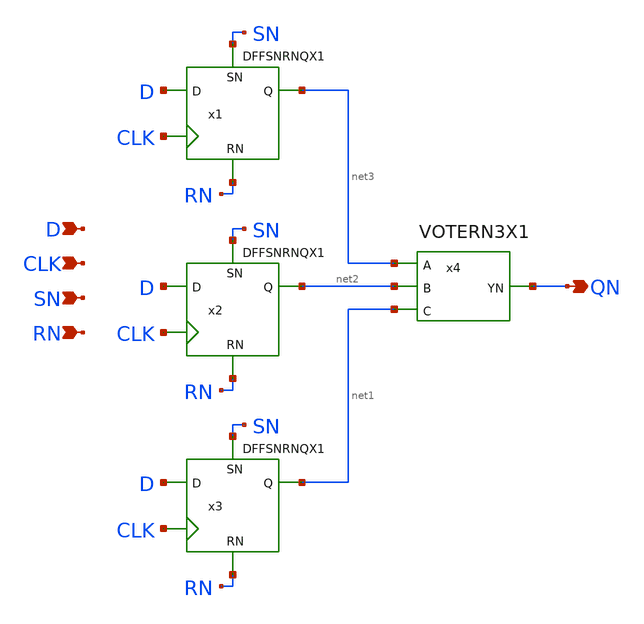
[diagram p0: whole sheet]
** sch_path: lib/xschem/TMRDFFSNRNQNX1.sch
**.subckt TMRDFFSNRNQNX1 QN D CLK SN RN
*.opin QN
*.ipin D
*.ipin CLK
*.ipin SN
*.ipin RN
x4 net3 net2 net1 QN VDD VSS VOTERN3X1
x1 net3 D CLK SN RN VDD VSS DFFSNRNQX1
x2 net2 D CLK SN RN VDD VSS DFFSNRNQX1
x3 net1 D CLK SN RN VDD VSS DFFSNRNQX1
**.ends
.end
